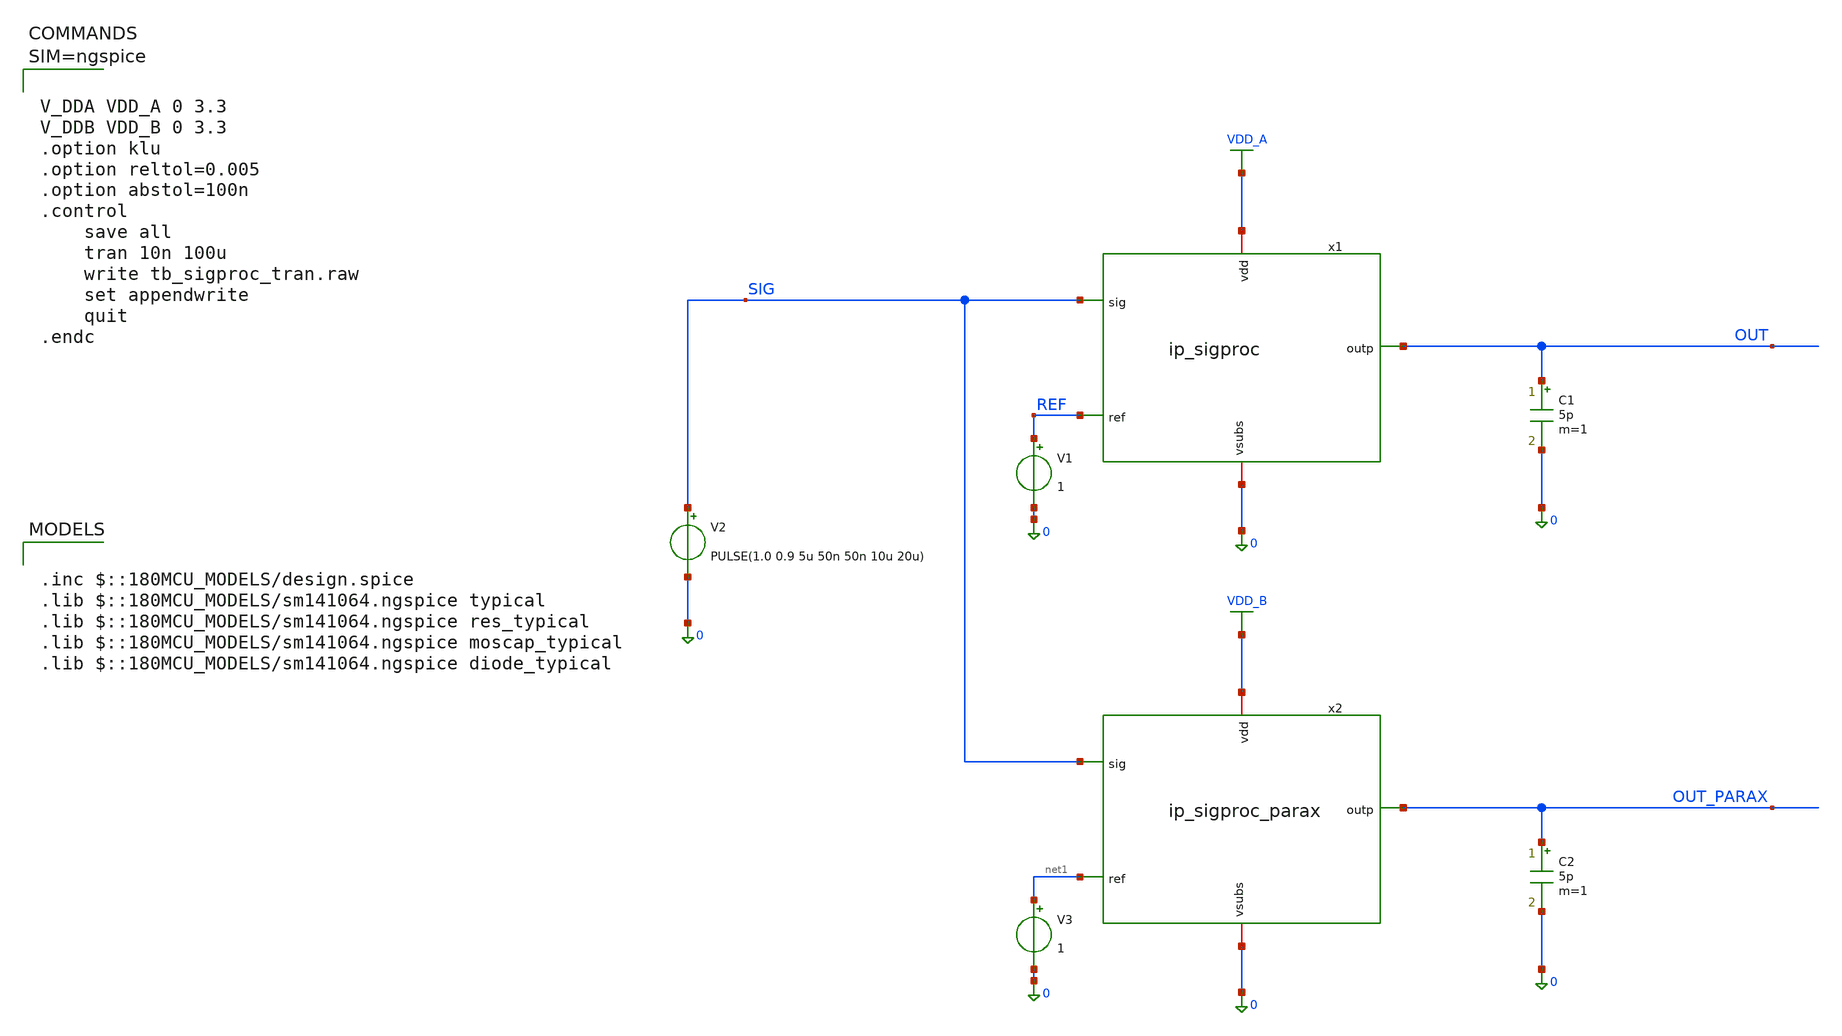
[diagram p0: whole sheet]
** sch_path: xschem/tb_sigproc_tran.sch
**.subckt tb_sigproc_tran
V2 SIG 0 PULSE(1.0 0.9 5u 50n 50n 10u 20u)
x1 VDD_A OUT SIG REF 0 ip_sigproc
V1 REF 0 1
C1 OUT 0 5p m=1
x2 VDD_B OUT_PARAX SIG net1 0 ip_sigproc_parax
V3 net1 0 1
C2 OUT_PARAX 0 5p m=1
**** begin user architecture code

.inc $::180MCU_MODELS/design.spice
.lib $::180MCU_MODELS/sm141064.ngspice typical
.lib $::180MCU_MODELS/sm141064.ngspice res_typical
.lib $::180MCU_MODELS/sm141064.ngspice moscap_typical
.lib $::180MCU_MODELS/sm141064.ngspice diode_typical




V_DDA VDD_A 0 3.3
V_DDB VDD_B 0 3.3
.option klu
.option reltol=0.005
.option abstol=100n
.control
	save all
	tran 10n 100u
	write tb_sigproc_tran.raw
	set appendwrite
	quit
.endc



**** end user architecture code
**.ends

* expanding   symbol:  ip_sigproc.sym # of pins=5
** sym_path: xschem/ip_sigproc.sym
** sch_path: xschem/ip_sigproc.sch
.subckt ip_sigproc vdd outp sig ref vsubs
*.ipin sig
*.ipin ref
*.iopin vdd
*.iopin vsubs
*.opin outp
x1 vdd net1 sig net1 vsubs ip_amplifier
x2 vdd outp ref net2 net6 ip_amplifier
XR1 net1 net2 net7 ppolyf_u_1k r_width=1e-6 r_length=10e-6 m=1
XR2 net2 net3 net8 ppolyf_u_1k r_width=1e-6 r_length=10e-6 m=1
XR3 net3 net4 net9 ppolyf_u_1k r_width=1e-6 r_length=10e-6 m=1
XR4 net4 net5 net10 ppolyf_u_1k r_width=1e-6 r_length=10e-6 m=1
XR5 net5 outp net11 ppolyf_u_1k r_width=1e-6 r_length=10e-6 m=1
XC1 outp net2 cap_pmos_03v3 c_width=12e-6 c_length=12e-6 m=1
XC2 net2 outp cap_pmos_03v3 c_width=12e-6 c_length=12e-6 m=1
.ends


* expanding   symbol:  ip_sigproc_parax.sym # of pins=5
** sym_path: xschem/ip_sigproc.sym
.include [file normalize ./parax/ip_sigproc.sim.spice]

* expanding   symbol:  xschem/ip_amplifier.sym # of pins=5
** sym_path: xschem/ip_amplifier.sym
** sch_path: xschem/ip_amplifier.sch
.subckt ip_amplifier VDD OUTP INP INN VSUBS
*.iopin VDD
*.iopin VSUBS
*.ipin INP
*.ipin INN
*.opin OUTP
XM1 net10 INP net8 VDD pfet_06v0 L=0.7u W=11.0u nf=1 ad='int((nf+1)/2) * W/nf * 0.18u' as='int((nf+2)/2) * W/nf * 0.18u'
+ pd='2*int((nf+1)/2) * (W/nf + 0.18u)' ps='2*int((nf+2)/2) * (W/nf + 0.18u)' nrd='0.18u / W' nrs='0.18u / W'
+ sa=0 sb=0 sd=0 m=2 par=2
XM2 net9 INN net8 VDD pfet_06v0 L=0.7u W=11.0u nf=1 ad='int((nf+1)/2) * W/nf * 0.18u' as='int((nf+2)/2) * W/nf * 0.18u'
+ pd='2*int((nf+1)/2) * (W/nf + 0.18u)' ps='2*int((nf+2)/2) * (W/nf + 0.18u)' nrd='0.18u / W' nrs='0.18u / W'
+ sa=0 sb=0 sd=0 m=2 par=2
XM5 net10 net1 VSUBS vsubs nfet_06v0 L=2u W=5u nf=1 ad='int((nf+1)/2) * W/nf * 0.18u' as='int((nf+2)/2) * W/nf * 0.18u'
+ pd='2*int((nf+1)/2) * (W/nf + 0.18u)' ps='2*int((nf+2)/2) * (W/nf + 0.18u)' nrd='0.18u / W' nrs='0.18u / W'
+ sa=0 sb=0 sd=0 m=1 par=1
XM6 net9 net1 VSUBS vsubs nfet_06v0 L=2u W=5u nf=1 ad='int((nf+1)/2) * W/nf * 0.18u' as='int((nf+2)/2) * W/nf * 0.18u'
+ pd='2*int((nf+1)/2) * (W/nf + 0.18u)' ps='2*int((nf+2)/2) * (W/nf + 0.18u)' nrd='0.18u / W' nrs='0.18u / W'
+ sa=0 sb=0 sd=0 m=1 par=1
XM3 net3 net1 VSUBS vsubs nfet_06v0 L=1u W=12.5u nf=1 ad='int((nf+1)/2) * W/nf * 0.18u' as='int((nf+2)/2) * W/nf * 0.18u'
+ pd='2*int((nf+1)/2) * (W/nf + 0.18u)' ps='2*int((nf+2)/2) * (W/nf + 0.18u)' nrd='0.18u / W' nrs='0.18u / W'
+ sa=0 sb=0 sd=0 m=2 par=2
XM4 net2 net1 VSUBS vsubs nfet_06v0 L=1u W=5u nf=1 ad='int((nf+1)/2) * W/nf * 0.18u' as='int((nf+2)/2) * W/nf * 0.18u'
+ pd='2*int((nf+1)/2) * (W/nf + 0.18u)' ps='2*int((nf+2)/2) * (W/nf + 0.18u)' nrd='0.18u / W' nrs='0.18u / W'
+ sa=0 sb=0 sd=0 m=1 par=1
XM7 net1 net1 net3 vsubs nfet_06v0 L=0.7u W=14u nf=1 ad='int((nf+1)/2) * W/nf * 0.18u' as='int((nf+2)/2) * W/nf * 0.18u'
+ pd='2*int((nf+1)/2) * (W/nf + 0.18u)' ps='2*int((nf+2)/2) * (W/nf + 0.18u)' nrd='0.18u / W' nrs='0.18u / W'
+ sa=0 sb=0 sd=0 m=2 par=2
XM8 net4 net1 net2 vsubs nfet_06v0 L=0.7u W=14u nf=1 ad='int((nf+1)/2) * W/nf * 0.18u' as='int((nf+2)/2) * W/nf * 0.18u'
+ pd='2*int((nf+1)/2) * (W/nf + 0.18u)' ps='2*int((nf+2)/2) * (W/nf + 0.18u)' nrd='0.18u / W' nrs='0.18u / W'
+ sa=0 sb=0 sd=0 m=2 par=2
XM9 net5 net7 VDD VDD pfet_06v0 L=1u W=6u nf=1 ad='int((nf+1)/2) * W/nf * 0.18u' as='int((nf+2)/2) * W/nf * 0.18u'
+ pd='2*int((nf+1)/2) * (W/nf + 0.18u)' ps='2*int((nf+2)/2) * (W/nf + 0.18u)' nrd='0.18u / W' nrs='0.18u / W'
+ sa=0 sb=0 sd=0 m=1 par=1
XM10 net6 net7 VDD VDD pfet_06v0 L=1u W=6u nf=1 ad='int((nf+1)/2) * W/nf * 0.18u' as='int((nf+2)/2) * W/nf * 0.18u'
+ pd='2*int((nf+1)/2) * (W/nf + 0.18u)' ps='2*int((nf+2)/2) * (W/nf + 0.18u)' nrd='0.18u / W' nrs='0.18u / W'
+ sa=0 sb=0 sd=0 m=1 par=1
XM11 net7 net7 net5 VDD pfet_06v0 L=0.7u W=14u nf=1 ad='int((nf+1)/2) * W/nf * 0.18u' as='int((nf+2)/2) * W/nf * 0.18u'
+ pd='2*int((nf+1)/2) * (W/nf + 0.18u)' ps='2*int((nf+2)/2) * (W/nf + 0.18u)' nrd='0.18u / W' nrs='0.18u / W'
+ sa=0 sb=0 sd=0 m=2 par=2
XM12 net8 net7 net6 VDD pfet_06v0 L=0.7u W=14u nf=1 ad='int((nf+1)/2) * W/nf * 0.18u' as='int((nf+2)/2) * W/nf * 0.18u'
+ pd='2*int((nf+1)/2) * (W/nf + 0.18u)' ps='2*int((nf+2)/2) * (W/nf + 0.18u)' nrd='0.18u / W' nrs='0.18u / W'
+ sa=0 sb=0 sd=0 m=2 par=2
XM13 net11 net1 net9 vsubs nfet_06v0 L=0.7u W=12u nf=1 ad='int((nf+1)/2) * W/nf * 0.18u' as='int((nf+2)/2) * W/nf * 0.18u'
+ pd='2*int((nf+1)/2) * (W/nf + 0.18u)' ps='2*int((nf+2)/2) * (W/nf + 0.18u)' nrd='0.18u / W' nrs='0.18u / W'
+ sa=0 sb=0 sd=0 m=1 par=1
XM14 COMP net1 net10 vsubs nfet_06v0 L=0.7u W=12u nf=1 ad='int((nf+1)/2) * W/nf * 0.18u' as='int((nf+2)/2) * W/nf * 0.18u'
+ pd='2*int((nf+1)/2) * (W/nf + 0.18u)' ps='2*int((nf+2)/2) * (W/nf + 0.18u)' nrd='0.18u / W' nrs='0.18u / W'
+ sa=0 sb=0 sd=0 m=1 par=1
XM15 net11 net11 VDD VDD pfet_06v0 L=0.7u W=12u nf=1 ad='int((nf+1)/2) * W/nf * 0.18u' as='int((nf+2)/2) * W/nf * 0.18u'
+ pd='2*int((nf+1)/2) * (W/nf + 0.18u)' ps='2*int((nf+2)/2) * (W/nf + 0.18u)' nrd='0.18u / W' nrs='0.18u / W'
+ sa=0 sb=0 sd=0 m=1 par=1
XM16 COMP net11 VDD VDD pfet_06v0 L=0.7u W=12u nf=1 ad='int((nf+1)/2) * W/nf * 0.18u' as='int((nf+2)/2) * W/nf * 0.18u'
+ pd='2*int((nf+1)/2) * (W/nf + 0.18u)' ps='2*int((nf+2)/2) * (W/nf + 0.18u)' nrd='0.18u / W' nrs='0.18u / W'
+ sa=0 sb=0 sd=0 m=1 par=1
XM17 OUTP COMP VDD VDD pfet_06v0 L=0.7u W=12u nf=1 ad='int((nf+1)/2) * W/nf * 0.18u' as='int((nf+2)/2) * W/nf * 0.18u'
+ pd='2*int((nf+1)/2) * (W/nf + 0.18u)' ps='2*int((nf+2)/2) * (W/nf + 0.18u)' nrd='0.18u / W' nrs='0.18u / W'
+ sa=0 sb=0 sd=0 m=5 par=5
XM18 OUTP net10 VSUBS vsubs nfet_06v0 L=0.7u W=12u nf=1 ad='int((nf+1)/2) * W/nf * 0.18u' as='int((nf+2)/2) * W/nf * 0.18u'
+ pd='2*int((nf+1)/2) * (W/nf + 0.18u)' ps='2*int((nf+2)/2) * (W/nf + 0.18u)' nrd='0.18u / W' nrs='0.18u / W'
+ sa=0 sb=0 sd=0 m=3 par=3
XR3 net1 net14 vsubs ppolyf_u_1k_6p0 r_width=1e-6 r_length=6e-6 m=1
XR6 net14 net13 vsubs ppolyf_u_1k_6p0 r_width=1e-6 r_length=6e-6 m=1
XR7 net13 net12 vsubs ppolyf_u_1k_6p0 r_width=1e-6 r_length=6e-6 m=1
XR8 net12 net15 vsubs ppolyf_u_1k_6p0 r_width=1e-6 r_length=4e-6 m=1
Vmeas VDD net15 0
Vmeas1 net7 net4 0
XC1 OUTP net16 cap_nmos_03v3 c_width=12e-6 c_length=18e-6 m=1
XC2 COMP net17 cap_nmos_03v3 c_width=12e-6 c_length=18e-6 m=1
XR12 net16 COMP vsubs ppolyf_u_1k_6p0 r_width=1e-6 r_length=10e-6 m=1
XR16 OUTP net17 vsubs ppolyf_u_1k_6p0 r_width=1e-6 r_length=10e-6 m=1
.ends

.GLOBAL VDD_A
.GLOBAL VDD_B
.end
